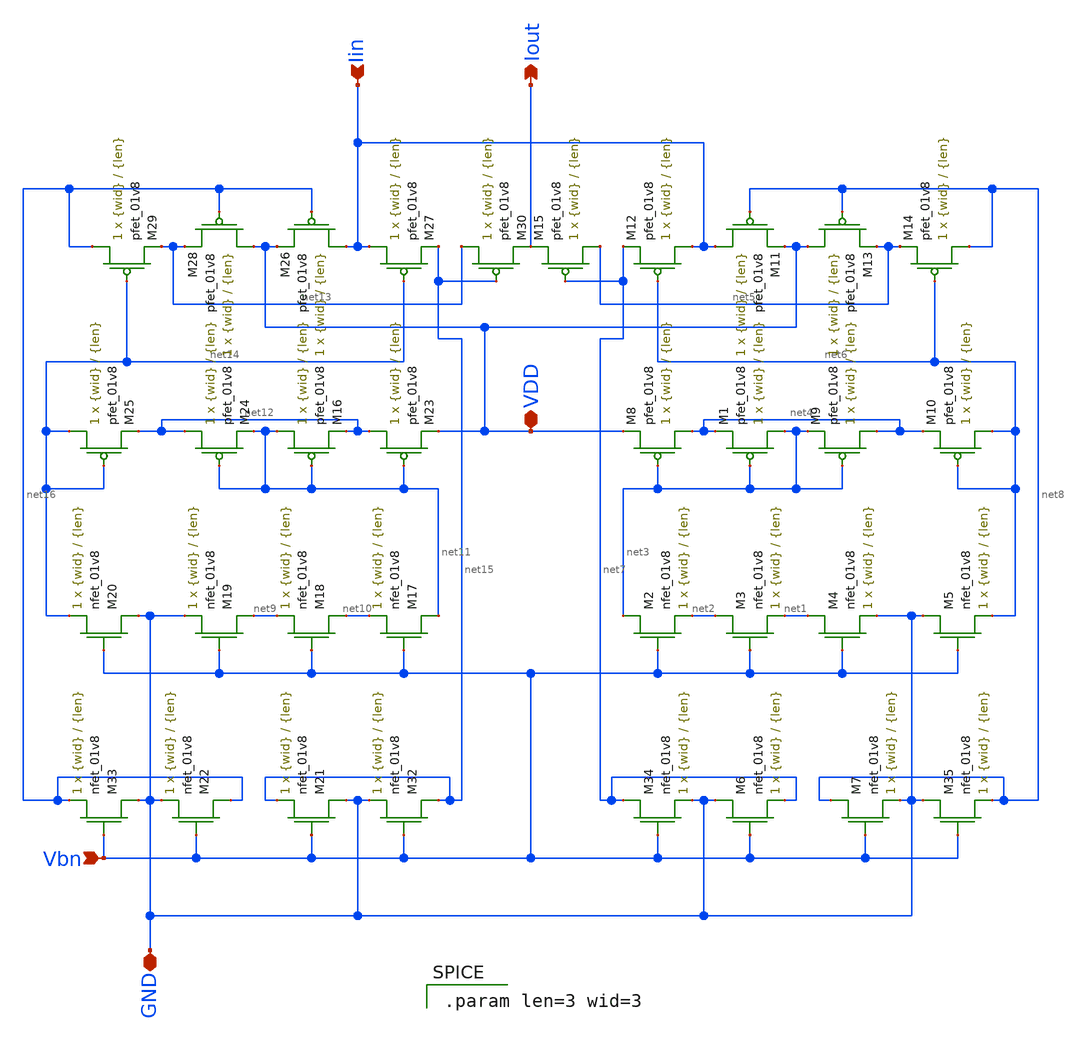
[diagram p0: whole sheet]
** sch_path: mp3/Layout_Schem_Designs/mirror_lds.sch
**.subckt mirror_lds Iin VDD Iout GND Vbn
*.ipin Iin
*.iopin VDD
*.opin Iout
*.iopin GND
*.ipin Vbn
XM1 net3 net3 net4 VDD sky130_fd_pr__pfet_01v8 L={len} W={wid} nf=1 ad='int((nf+1)/2) * W/nf * 0.29'
+ as='int((nf+2)/2) * W/nf * 0.29' pd='2*int((nf+1)/2) * (W/nf + 0.29)' ps='2*int((nf+2)/2) * (W/nf + 0.29)'
+ nrd='0.29 / W' nrs='0.29 / W' sa=0 sb=0 sd=0 mult=1 m=1
XM2 net3 Vbn net2 GND sky130_fd_pr__nfet_01v8 L={len} W={wid} nf=1 ad='int((nf+1)/2) * W/nf * 0.29' as='int((nf+2)/2) * W/nf * 0.29'
+ pd='2*int((nf+1)/2) * (W/nf + 0.29)' ps='2*int((nf+2)/2) * (W/nf + 0.29)' nrd='0.29 / W' nrs='0.29 / W'
+ sa=0 sb=0 sd=0 mult=1 m=1
XM3 net2 Vbn net1 GND sky130_fd_pr__nfet_01v8 L={len} W={wid} nf=1 ad='int((nf+1)/2) * W/nf * 0.29' as='int((nf+2)/2) * W/nf * 0.29'
+ pd='2*int((nf+1)/2) * (W/nf + 0.29)' ps='2*int((nf+2)/2) * (W/nf + 0.29)' nrd='0.29 / W' nrs='0.29 / W'
+ sa=0 sb=0 sd=0 mult=1 m=1
XM4 net1 Vbn GND GND sky130_fd_pr__nfet_01v8 L={len} W={wid} nf=1 ad='int((nf+1)/2) * W/nf * 0.29' as='int((nf+2)/2) * W/nf * 0.29'
+ pd='2*int((nf+1)/2) * (W/nf + 0.29)' ps='2*int((nf+2)/2) * (W/nf + 0.29)' nrd='0.29 / W' nrs='0.29 / W'
+ sa=0 sb=0 sd=0 mult=1 m=1
XM5 GND Vbn net6 GND sky130_fd_pr__nfet_01v8 L={len} W={wid} nf=1 ad='int((nf+1)/2) * W/nf * 0.29' as='int((nf+2)/2) * W/nf * 0.29'
+ pd='2*int((nf+1)/2) * (W/nf + 0.29)' ps='2*int((nf+2)/2) * (W/nf + 0.29)' nrd='0.29 / W' nrs='0.29 / W'
+ sa=0 sb=0 sd=0 mult=1 m=1
XM8 net4 net3 VDD VDD sky130_fd_pr__pfet_01v8 L={len} W={wid} nf=1 ad='int((nf+1)/2) * W/nf * 0.29' as='int((nf+2)/2) * W/nf * 0.29'
+ pd='2*int((nf+1)/2) * (W/nf + 0.29)' ps='2*int((nf+2)/2) * (W/nf + 0.29)' nrd='0.29 / W' nrs='0.29 / W'
+ sa=0 sb=0 sd=0 mult=1 m=1
XM9 net4 net3 net3 VDD sky130_fd_pr__pfet_01v8 L={len} W={wid} nf=1 ad='int((nf+1)/2) * W/nf * 0.29'
+ as='int((nf+2)/2) * W/nf * 0.29' pd='2*int((nf+1)/2) * (W/nf + 0.29)' ps='2*int((nf+2)/2) * (W/nf + 0.29)'
+ nrd='0.29 / W' nrs='0.29 / W' sa=0 sb=0 sd=0 mult=1 m=1
XM10 net6 net6 net4 VDD sky130_fd_pr__pfet_01v8 L={len} W={wid} nf=1 ad='int((nf+1)/2) * W/nf * 0.29'
+ as='int((nf+2)/2) * W/nf * 0.29' pd='2*int((nf+1)/2) * (W/nf + 0.29)' ps='2*int((nf+2)/2) * (W/nf + 0.29)'
+ nrd='0.29 / W' nrs='0.29 / W' sa=0 sb=0 sd=0 mult=1 m=1
XM11 Iin net8 VDD VDD sky130_fd_pr__pfet_01v8 L={len} W={wid} nf=1 ad='int((nf+1)/2) * W/nf * 0.29' as='int((nf+2)/2) * W/nf * 0.29'
+ pd='2*int((nf+1)/2) * (W/nf + 0.29)' ps='2*int((nf+2)/2) * (W/nf + 0.29)' nrd='0.29 / W' nrs='0.29 / W'
+ sa=0 sb=0 sd=0 mult=1 m=1
XM12 Iin net6 net7 VDD sky130_fd_pr__pfet_01v8 L={len} W={wid} nf=1 ad='int((nf+1)/2) * W/nf * 0.29'
+ as='int((nf+2)/2) * W/nf * 0.29' pd='2*int((nf+1)/2) * (W/nf + 0.29)' ps='2*int((nf+2)/2) * (W/nf + 0.29)'
+ nrd='0.29 / W' nrs='0.29 / W' sa=0 sb=0 sd=0 mult=1 m=1
XM13 VDD net8 net5 VDD sky130_fd_pr__pfet_01v8 L={len} W={wid} nf=1 ad='int((nf+1)/2) * W/nf * 0.29'
+ as='int((nf+2)/2) * W/nf * 0.29' pd='2*int((nf+1)/2) * (W/nf + 0.29)' ps='2*int((nf+2)/2) * (W/nf + 0.29)'
+ nrd='0.29 / W' nrs='0.29 / W' sa=0 sb=0 sd=0 mult=1 m=1
XM14 net8 net6 net5 VDD sky130_fd_pr__pfet_01v8 L={len} W={wid} nf=1 ad='int((nf+1)/2) * W/nf * 0.29'
+ as='int((nf+2)/2) * W/nf * 0.29' pd='2*int((nf+1)/2) * (W/nf + 0.29)' ps='2*int((nf+2)/2) * (W/nf + 0.29)'
+ nrd='0.29 / W' nrs='0.29 / W' sa=0 sb=0 sd=0 mult=1 m=1
XM15 net5 net7 Iout VDD sky130_fd_pr__pfet_01v8 L={len} W={wid} nf=1 ad='int((nf+1)/2) * W/nf * 0.29'
+ as='int((nf+2)/2) * W/nf * 0.29' pd='2*int((nf+1)/2) * (W/nf + 0.29)' ps='2*int((nf+2)/2) * (W/nf + 0.29)'
+ nrd='0.29 / W' nrs='0.29 / W' sa=0 sb=0 sd=0 mult=1 m=1
XM16 net11 net11 net12 VDD sky130_fd_pr__pfet_01v8 L={len} W={wid} nf=1 ad='int((nf+1)/2) * W/nf * 0.29'
+ as='int((nf+2)/2) * W/nf * 0.29' pd='2*int((nf+1)/2) * (W/nf + 0.29)' ps='2*int((nf+2)/2) * (W/nf + 0.29)'
+ nrd='0.29 / W' nrs='0.29 / W' sa=0 sb=0 sd=0 mult=1 m=1
XM17 net11 Vbn net10 GND sky130_fd_pr__nfet_01v8 L={len} W={wid} nf=1 ad='int((nf+1)/2) * W/nf * 0.29'
+ as='int((nf+2)/2) * W/nf * 0.29' pd='2*int((nf+1)/2) * (W/nf + 0.29)' ps='2*int((nf+2)/2) * (W/nf + 0.29)'
+ nrd='0.29 / W' nrs='0.29 / W' sa=0 sb=0 sd=0 mult=1 m=1
XM18 net10 Vbn net9 GND sky130_fd_pr__nfet_01v8 L={len} W={wid} nf=1 ad='int((nf+1)/2) * W/nf * 0.29'
+ as='int((nf+2)/2) * W/nf * 0.29' pd='2*int((nf+1)/2) * (W/nf + 0.29)' ps='2*int((nf+2)/2) * (W/nf + 0.29)'
+ nrd='0.29 / W' nrs='0.29 / W' sa=0 sb=0 sd=0 mult=1 m=1
XM19 net9 Vbn GND GND sky130_fd_pr__nfet_01v8 L={len} W={wid} nf=1 ad='int((nf+1)/2) * W/nf * 0.29' as='int((nf+2)/2) * W/nf * 0.29'
+ pd='2*int((nf+1)/2) * (W/nf + 0.29)' ps='2*int((nf+2)/2) * (W/nf + 0.29)' nrd='0.29 / W' nrs='0.29 / W'
+ sa=0 sb=0 sd=0 mult=1 m=1
XM20 GND Vbn net14 GND sky130_fd_pr__nfet_01v8 L={len} W={wid} nf=1 ad='int((nf+1)/2) * W/nf * 0.29'
+ as='int((nf+2)/2) * W/nf * 0.29' pd='2*int((nf+1)/2) * (W/nf + 0.29)' ps='2*int((nf+2)/2) * (W/nf + 0.29)'
+ nrd='0.29 / W' nrs='0.29 / W' sa=0 sb=0 sd=0 mult=1 m=1
XM23 net12 net11 VDD VDD sky130_fd_pr__pfet_01v8 L={len} W={wid} nf=1 ad='int((nf+1)/2) * W/nf * 0.29'
+ as='int((nf+2)/2) * W/nf * 0.29' pd='2*int((nf+1)/2) * (W/nf + 0.29)' ps='2*int((nf+2)/2) * (W/nf + 0.29)'
+ nrd='0.29 / W' nrs='0.29 / W' sa=0 sb=0 sd=0 mult=1 m=1
XM24 net12 net11 net11 VDD sky130_fd_pr__pfet_01v8 L={len} W={wid} nf=1 ad='int((nf+1)/2) * W/nf * 0.29'
+ as='int((nf+2)/2) * W/nf * 0.29' pd='2*int((nf+1)/2) * (W/nf + 0.29)' ps='2*int((nf+2)/2) * (W/nf + 0.29)'
+ nrd='0.29 / W' nrs='0.29 / W' sa=0 sb=0 sd=0 mult=1 m=1
XM25 net14 net14 net12 VDD sky130_fd_pr__pfet_01v8 L={len} W={wid} nf=1 ad='int((nf+1)/2) * W/nf * 0.29'
+ as='int((nf+2)/2) * W/nf * 0.29' pd='2*int((nf+1)/2) * (W/nf + 0.29)' ps='2*int((nf+2)/2) * (W/nf + 0.29)'
+ nrd='0.29 / W' nrs='0.29 / W' sa=0 sb=0 sd=0 mult=1 m=1
XM26 Iin net16 VDD VDD sky130_fd_pr__pfet_01v8 L={len} W={wid} nf=1 ad='int((nf+1)/2) * W/nf * 0.29'
+ as='int((nf+2)/2) * W/nf * 0.29' pd='2*int((nf+1)/2) * (W/nf + 0.29)' ps='2*int((nf+2)/2) * (W/nf + 0.29)'
+ nrd='0.29 / W' nrs='0.29 / W' sa=0 sb=0 sd=0 mult=1 m=1
XM27 Iin net14 net15 VDD sky130_fd_pr__pfet_01v8 L={len} W={wid} nf=1 ad='int((nf+1)/2) * W/nf * 0.29'
+ as='int((nf+2)/2) * W/nf * 0.29' pd='2*int((nf+1)/2) * (W/nf + 0.29)' ps='2*int((nf+2)/2) * (W/nf + 0.29)'
+ nrd='0.29 / W' nrs='0.29 / W' sa=0 sb=0 sd=0 mult=1 m=1
XM28 VDD net16 net13 VDD sky130_fd_pr__pfet_01v8 L={len} W={wid} nf=1 ad='int((nf+1)/2) * W/nf * 0.29'
+ as='int((nf+2)/2) * W/nf * 0.29' pd='2*int((nf+1)/2) * (W/nf + 0.29)' ps='2*int((nf+2)/2) * (W/nf + 0.29)'
+ nrd='0.29 / W' nrs='0.29 / W' sa=0 sb=0 sd=0 mult=1 m=1
XM29 net16 net14 net13 VDD sky130_fd_pr__pfet_01v8 L={len} W={wid} nf=1 ad='int((nf+1)/2) * W/nf * 0.29'
+ as='int((nf+2)/2) * W/nf * 0.29' pd='2*int((nf+1)/2) * (W/nf + 0.29)' ps='2*int((nf+2)/2) * (W/nf + 0.29)'
+ nrd='0.29 / W' nrs='0.29 / W' sa=0 sb=0 sd=0 mult=1 m=1
XM30 net13 net15 Iout VDD sky130_fd_pr__pfet_01v8 L={len} W={wid} nf=1 ad='int((nf+1)/2) * W/nf * 0.29'
+ as='int((nf+2)/2) * W/nf * 0.29' pd='2*int((nf+1)/2) * (W/nf + 0.29)' ps='2*int((nf+2)/2) * (W/nf + 0.29)'
+ nrd='0.29 / W' nrs='0.29 / W' sa=0 sb=0 sd=0 mult=1 m=1
XM21 GND Vbn net15 GND sky130_fd_pr__nfet_01v8 L={len} W={wid} nf=1 ad='int((nf+1)/2) * W/nf * 0.29'
+ as='int((nf+2)/2) * W/nf * 0.29' pd='2*int((nf+1)/2) * (W/nf + 0.29)' ps='2*int((nf+2)/2) * (W/nf + 0.29)'
+ nrd='0.29 / W' nrs='0.29 / W' sa=0 sb=0 sd=0 mult=1 m=1
XM22 net16 Vbn GND GND sky130_fd_pr__nfet_01v8 L={len} W={wid} nf=1 ad='int((nf+1)/2) * W/nf * 0.29'
+ as='int((nf+2)/2) * W/nf * 0.29' pd='2*int((nf+1)/2) * (W/nf + 0.29)' ps='2*int((nf+2)/2) * (W/nf + 0.29)'
+ nrd='0.29 / W' nrs='0.29 / W' sa=0 sb=0 sd=0 mult=1 m=1
XM32 net15 Vbn GND GND sky130_fd_pr__nfet_01v8 L={len} W={wid} nf=1 ad='int((nf+1)/2) * W/nf * 0.29'
+ as='int((nf+2)/2) * W/nf * 0.29' pd='2*int((nf+1)/2) * (W/nf + 0.29)' ps='2*int((nf+2)/2) * (W/nf + 0.29)'
+ nrd='0.29 / W' nrs='0.29 / W' sa=0 sb=0 sd=0 mult=1 m=1
XM33 GND Vbn net16 GND sky130_fd_pr__nfet_01v8 L={len} W={wid} nf=1 ad='int((nf+1)/2) * W/nf * 0.29'
+ as='int((nf+2)/2) * W/nf * 0.29' pd='2*int((nf+1)/2) * (W/nf + 0.29)' ps='2*int((nf+2)/2) * (W/nf + 0.29)'
+ nrd='0.29 / W' nrs='0.29 / W' sa=0 sb=0 sd=0 mult=1 m=1
XM6 GND Vbn net7 GND sky130_fd_pr__nfet_01v8 L={len} W={wid} nf=1 ad='int((nf+1)/2) * W/nf * 0.29' as='int((nf+2)/2) * W/nf * 0.29'
+ pd='2*int((nf+1)/2) * (W/nf + 0.29)' ps='2*int((nf+2)/2) * (W/nf + 0.29)' nrd='0.29 / W' nrs='0.29 / W'
+ sa=0 sb=0 sd=0 mult=1 m=1
XM7 net8 Vbn GND GND sky130_fd_pr__nfet_01v8 L={len} W={wid} nf=1 ad='int((nf+1)/2) * W/nf * 0.29' as='int((nf+2)/2) * W/nf * 0.29'
+ pd='2*int((nf+1)/2) * (W/nf + 0.29)' ps='2*int((nf+2)/2) * (W/nf + 0.29)' nrd='0.29 / W' nrs='0.29 / W'
+ sa=0 sb=0 sd=0 mult=1 m=1
XM34 net7 Vbn GND GND sky130_fd_pr__nfet_01v8 L={len} W={wid} nf=1 ad='int((nf+1)/2) * W/nf * 0.29' as='int((nf+2)/2) * W/nf * 0.29'
+ pd='2*int((nf+1)/2) * (W/nf + 0.29)' ps='2*int((nf+2)/2) * (W/nf + 0.29)' nrd='0.29 / W' nrs='0.29 / W'
+ sa=0 sb=0 sd=0 mult=1 m=1
XM35 GND Vbn net8 GND sky130_fd_pr__nfet_01v8 L={len} W={wid} nf=1 ad='int((nf+1)/2) * W/nf * 0.29' as='int((nf+2)/2) * W/nf * 0.29'
+ pd='2*int((nf+1)/2) * (W/nf + 0.29)' ps='2*int((nf+2)/2) * (W/nf + 0.29)' nrd='0.29 / W' nrs='0.29 / W'
+ sa=0 sb=0 sd=0 mult=1 m=1
**** begin user architecture code

.param len=3 wid=3

**** end user architecture code
**.ends
.end
